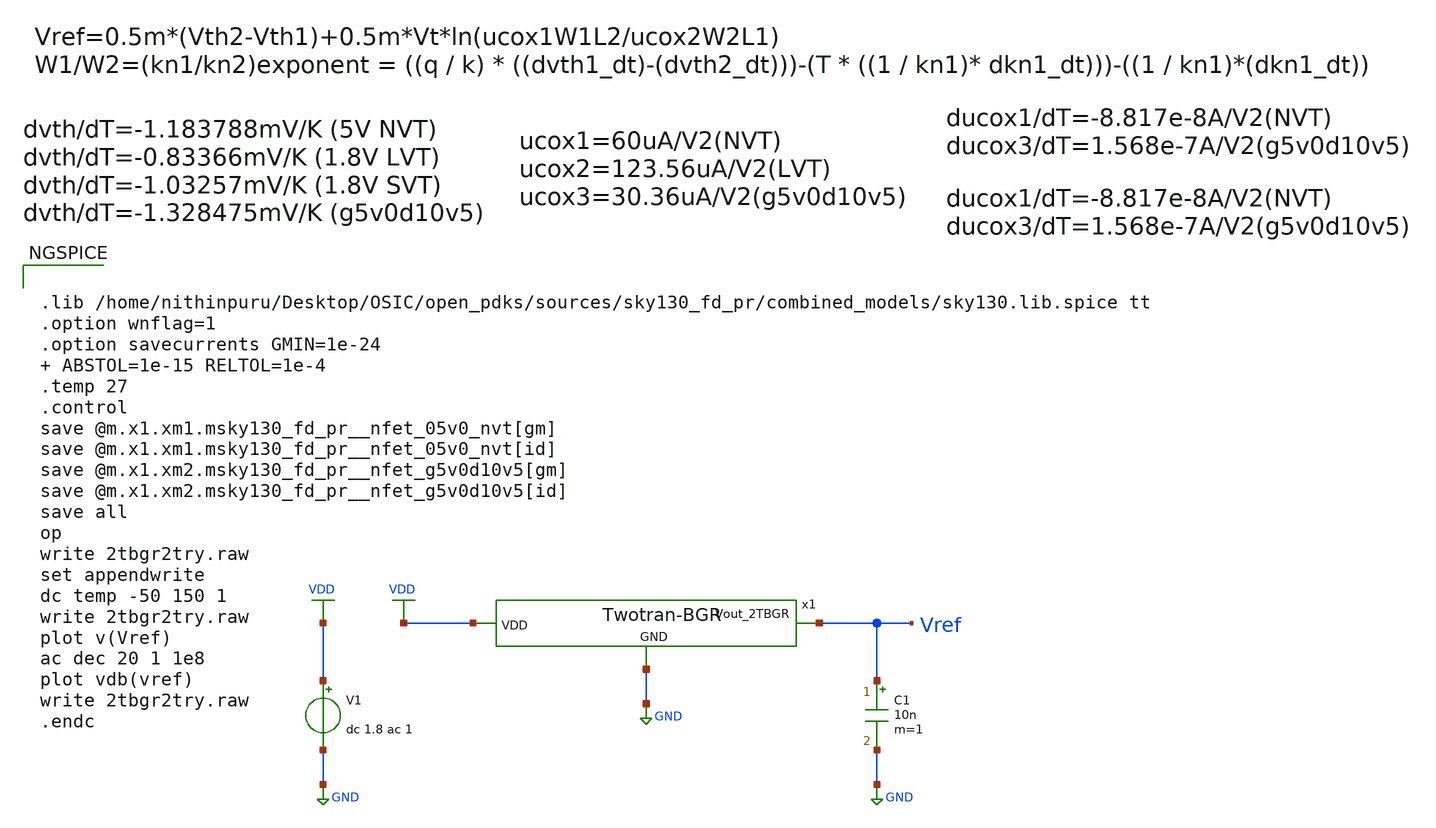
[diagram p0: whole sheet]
** sch_path: 2TBGR/Schematics/2tbgr2try.sch
**.subckt 2tbgr2try
V1 VDD GND dc 1.8 ac 1
x1 VDD GND Vref Twotran-BGR
C1 Vref GND 10n m=1
**** begin user architecture code


.lib /home/nithinpuru/Desktop/OSIC/open_pdks/sources/sky130_fd_pr/combined_models/sky130.lib.spice tt
.option wnflag=1
.option savecurrents GMIN=1e-24  ABSTOL=1e-15 RELTOL=1e-4
.temp 27
.control
save @m.x1.xm1.msky130_fd_pr__nfet_05v0_nvt[gm]
save @m.x1.xm1.msky130_fd_pr__nfet_05v0_nvt[id]
save @m.x1.xm2.msky130_fd_pr__nfet_g5v0d10v5[gm]
save @m.x1.xm2.msky130_fd_pr__nfet_g5v0d10v5[id]
save all
op
write 2tbgr2try.raw
set appendwrite
dc temp -50 150 1
write 2tbgr2try.raw
plot v(Vref)
ac dec 20 1 1e8
plot vdb(vref)
write 2tbgr2try.raw
.endc


**** end user architecture code
**.ends

* expanding   symbol:  Sims/IITGN/2TBGR/Twotran-BGR.sym # of pins=3
** sym_path: 2TBGR/Schematics/Twotran-BGR.sym
** sch_path: 2TBGR/Schematics/Twotran-BGR.sch
.subckt Twotran-BGR VDD GND Vout_2TBGR
*.ipin GND
*.ipin VDD
*.opin Vout_2TBGR
XM3 VDD GND Vout_2TBGR GND sky130_fd_pr__nfet_05v0_nvt L=20 W=17 nf=1 ad='int((nf+1)/2) * W/nf * 0.29'
+ as='int((nf+2)/2) * W/nf * 0.29' pd='2*int((nf+1)/2) * (W/nf + 0.29)' ps='2*int((nf+2)/2) * (W/nf + 0.29)'
+ nrd='0.29 / W' nrs='0.29 / W' sa=0 sb=0 sd=0 mult=1 m=1
XM1 Vout_2TBGR Vout_2TBGR GND GND sky130_fd_pr__nfet_g5v0d10v5 L=20 W=1 nf=1 ad='int((nf+1)/2) * W/nf * 0.29'
+ as='int((nf+2)/2) * W/nf * 0.29' pd='2*int((nf+1)/2) * (W/nf + 0.29)' ps='2*int((nf+2)/2) * (W/nf + 0.29)'
+ nrd='0.29 / W' nrs='0.29 / W' sa=0 sb=0 sd=0 mult=1 m=1
.ends

.GLOBAL GND
.GLOBAL VDD
.end
